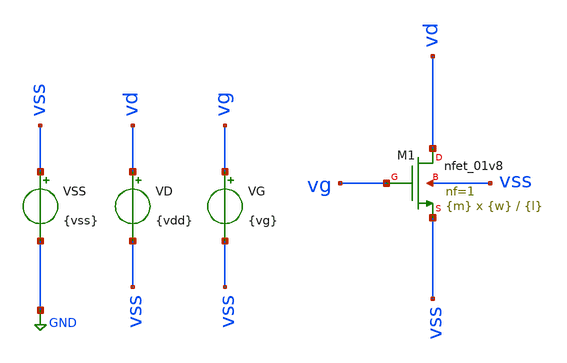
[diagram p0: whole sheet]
** sch_path: sch/nmos/nmos_simulation.sch
**.subckt nmos_simulation
XM1 vd vg vss vss sky130_fd_pr__nfet_01v8 L={l} W={w} nf=1 ad='int((nf+1)/2) * W/nf * 0.29' as='int((nf+2)/2) * W/nf * 0.29'
+ pd='2*int((nf+1)/2) * (W/nf + 0.29)' ps='2*int((nf+2)/2) * (W/nf + 0.29)' nrd='0.29 / W' nrs='0.29 / W'
+ sa=0 sb=0 sd=0 mult={m} m={m}
VG vg vss {vg}
VD vd vss {vdd}
VSS vss GND {vss}
**** begin user architecture code



* Parameters
.param vdd = 1.8
.param vss = 0.0
.param vg = 0.9
.param l = 0.15
.param w = 1.5
.param m = 1

.options TEMPS = 27.0

* Models
.lib ~/skywater/skywater-pdk/libraries/sky130_fd_pr_ngspice/latest/models/corners/sky130.lib FS

* Data to save
.save all  @M.XM1.msky130_fd_pr__nfet_01v8[id]

* Simulation
.control
  	dc VD 0 1.8 0.01 VG 0 1.8 0.3
	setplot dc1
	plot @M.XM1.msky130_fd_pr__nfet_01v8[id] xlabel Vds ylabel Id title 'Id vs Vds vs Vgs'
	set filetype = ascii
	write tp1_nmos_dc1.raw
.endc

.end


**** end user architecture code
**.ends
.GLOBAL GND
.end
